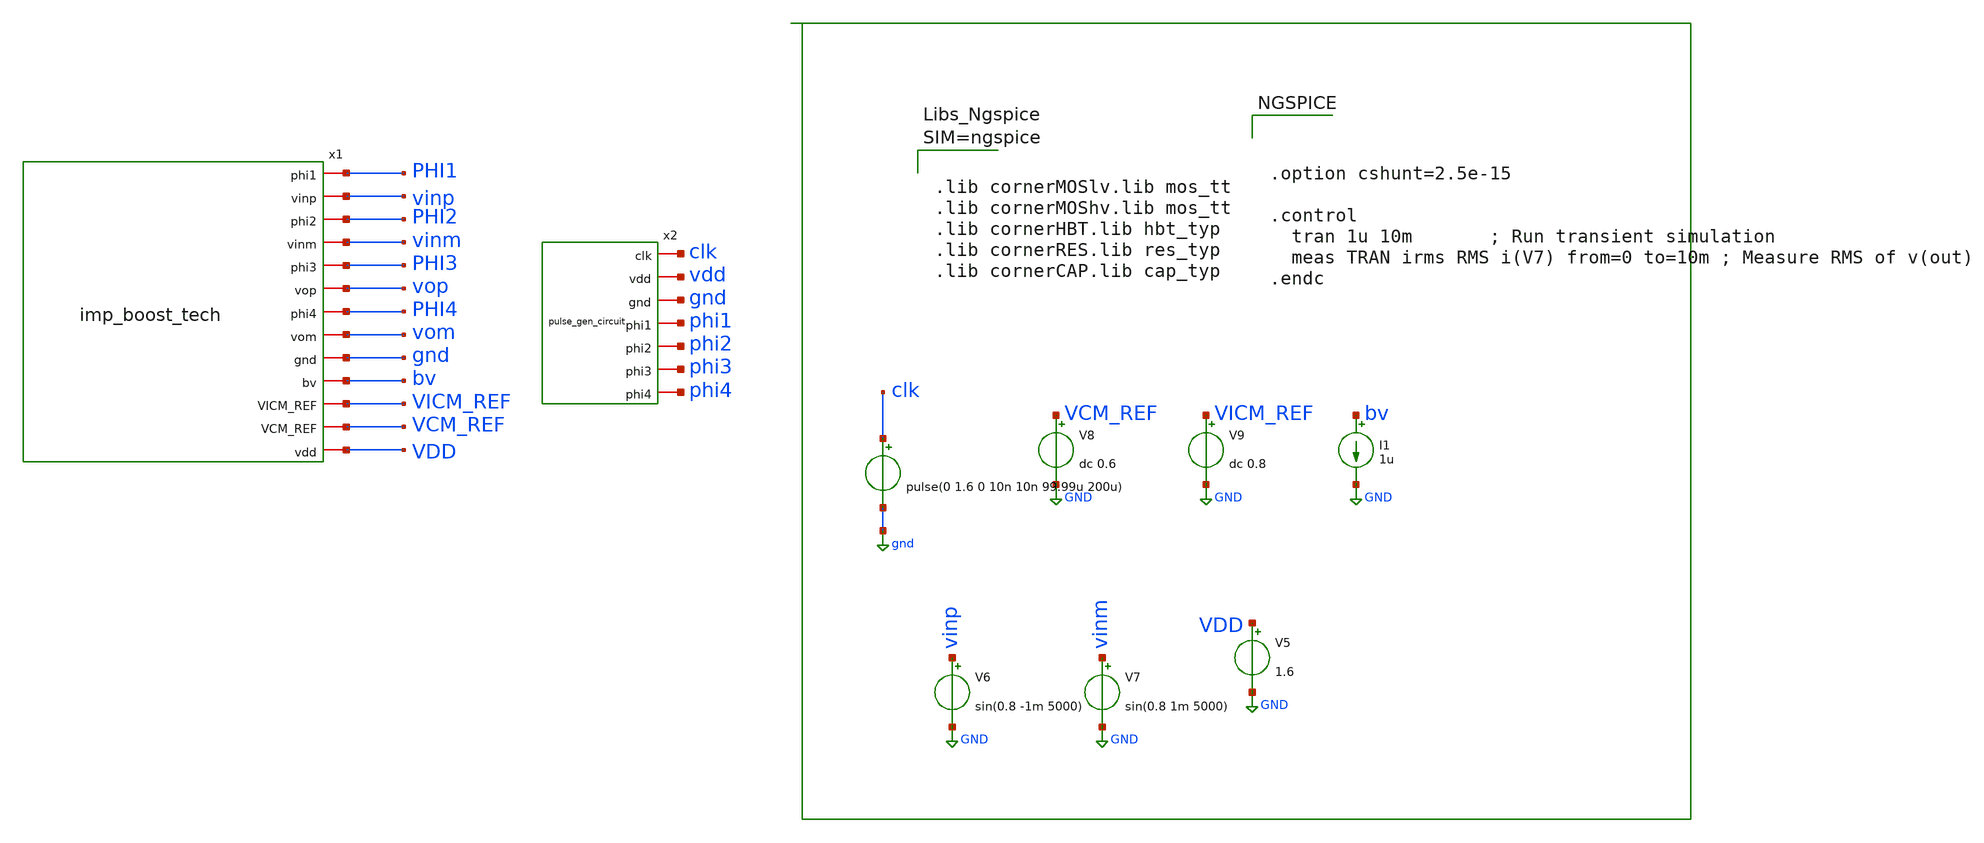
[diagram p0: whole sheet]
** sch_path: dependencies/OTA/OTA-main/schematic/xschem/test_input_imp.sch
**.subckt test_input_imp
V5 VDD GND 1.6
V8 VCM_REF GND dc 0.6
V9 VICM_REF GND dc 0.8
I1 bv GND 1u
x1 PHI1 vinp PHI2 vinm PHI3 vop PHI4 vom gnd bv VICM_REF VCM_REF VDD imp_boost_tech
V6 vinp GND sin(0.8 -1m 5000)
V7 vinm GND sin(0.8 1m 5000)
x2 clk vdd gnd phi1 phi2 phi3 phi4 pulse_gen_circuit
V1 clk gnd pulse(0 1.6 0 10n 10n 99.99u 200u)
**** begin user architecture code



.lib cornerMOSlv.lib mos_tt
.lib cornerMOShv.lib mos_tt
.lib cornerHBT.lib hbt_typ
.lib cornerRES.lib res_typ
.lib cornerCAP.lib cap_typ






.option cshunt=2.5e-15

.control
  tran 1u 10m       ; Run transient simulation
  meas TRAN irms RMS i(V7) from=0 to=10m ; Measure RMS of v(out)
.endc



**** end user architecture code
**.ends
.GLOBAL GND
.GLOBAL gnd
.end
